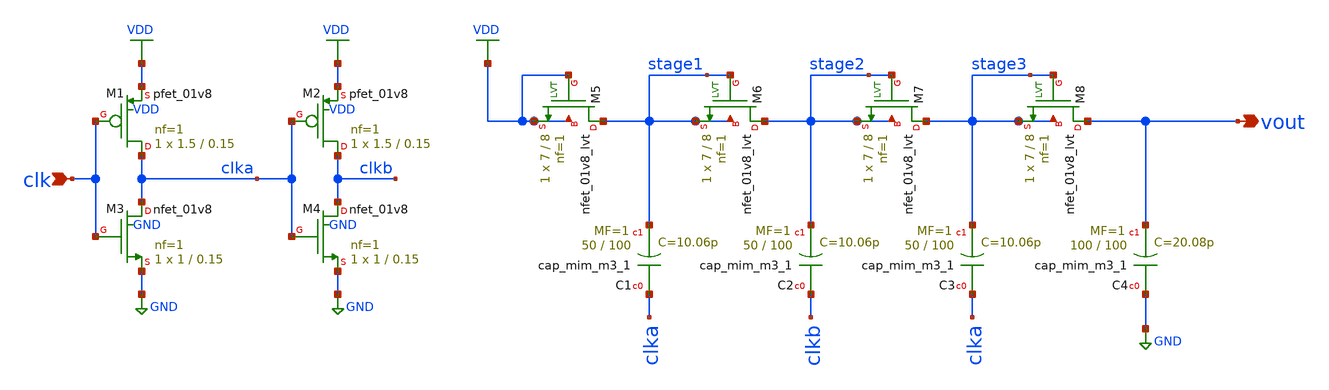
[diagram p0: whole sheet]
** sch_path: xschem/dickson.sch
**.subckt dickson clk vout
*.ipin clk
*.opin vout
XM1 clka clk VDD VDD sky130_fd_pr__pfet_01v8 L=0.15 W=1.5 nf=1 ad='int((nf+1)/2) * W/nf * 0.29' as='int((nf+2)/2) * W/nf * 0.29'
+ pd='2*int((nf+1)/2) * (W/nf + 0.29)' ps='2*int((nf+2)/2) * (W/nf + 0.29)' nrd='0.29 / W' nrs='0.29 / W'
+ sa=0 sb=0 sd=0 mult=1 m=1
XM3 clka clk GND GND sky130_fd_pr__nfet_01v8 L=0.15 W=1 nf=1 ad='int((nf+1)/2) * W/nf * 0.29' as='int((nf+2)/2) * W/nf * 0.29'
+ pd='2*int((nf+1)/2) * (W/nf + 0.29)' ps='2*int((nf+2)/2) * (W/nf + 0.29)' nrd='0.29 / W' nrs='0.29 / W'
+ sa=0 sb=0 sd=0 mult=1 m=1
XM2 clkb clka VDD VDD sky130_fd_pr__pfet_01v8 L=0.15 W=1.5 nf=1 ad='int((nf+1)/2) * W/nf * 0.29' as='int((nf+2)/2) * W/nf * 0.29'
+ pd='2*int((nf+1)/2) * (W/nf + 0.29)' ps='2*int((nf+2)/2) * (W/nf + 0.29)' nrd='0.29 / W' nrs='0.29 / W'
+ sa=0 sb=0 sd=0 mult=1 m=1
XM4 clkb clka GND GND sky130_fd_pr__nfet_01v8 L=0.15 W=1 nf=1 ad='int((nf+1)/2) * W/nf * 0.29' as='int((nf+2)/2) * W/nf * 0.29'
+ pd='2*int((nf+1)/2) * (W/nf + 0.29)' ps='2*int((nf+2)/2) * (W/nf + 0.29)' nrd='0.29 / W' nrs='0.29 / W'
+ sa=0 sb=0 sd=0 mult=1 m=1
XC3 clka stage3 sky130_fd_pr__cap_mim_m3_1 W=50 L=100 MF=1 m=1
XM5 stage1 VDD VDD VDD sky130_fd_pr__nfet_01v8_lvt L=8 W=7 nf=1 ad='int((nf+1)/2) * W/nf * 0.29' as='int((nf+2)/2) * W/nf * 0.29'
+ pd='2*int((nf+1)/2) * (W/nf + 0.29)' ps='2*int((nf+2)/2) * (W/nf + 0.29)' nrd='0.29 / W' nrs='0.29 / W'
+ sa=0 sb=0 sd=0 mult=1 m=1
XC1 clka stage1 sky130_fd_pr__cap_mim_m3_1 W=50 L=100 MF=1 m=1
XM6 stage2 stage1 stage1 stage1 sky130_fd_pr__nfet_01v8_lvt L=8 W=7 nf=1 ad='int((nf+1)/2) * W/nf * 0.29'
+ as='int((nf+2)/2) * W/nf * 0.29' pd='2*int((nf+1)/2) * (W/nf + 0.29)' ps='2*int((nf+2)/2) * (W/nf + 0.29)'
+ nrd='0.29 / W' nrs='0.29 / W' sa=0 sb=0 sd=0 mult=1 m=1
XM7 stage3 stage2 stage2 stage2 sky130_fd_pr__nfet_01v8_lvt L=8 W=7 nf=1 ad='int((nf+1)/2) * W/nf * 0.29'
+ as='int((nf+2)/2) * W/nf * 0.29' pd='2*int((nf+1)/2) * (W/nf + 0.29)' ps='2*int((nf+2)/2) * (W/nf + 0.29)'
+ nrd='0.29 / W' nrs='0.29 / W' sa=0 sb=0 sd=0 mult=1 m=1
XC2 clkb stage2 sky130_fd_pr__cap_mim_m3_1 W=50 L=100 MF=1 m=1
XM8 vout stage3 stage3 stage3 sky130_fd_pr__nfet_01v8_lvt L=8 W=7 nf=1 ad='int((nf+1)/2) * W/nf * 0.29'
+ as='int((nf+2)/2) * W/nf * 0.29' pd='2*int((nf+1)/2) * (W/nf + 0.29)' ps='2*int((nf+2)/2) * (W/nf + 0.29)'
+ nrd='0.29 / W' nrs='0.29 / W' sa=0 sb=0 sd=0 mult=1 m=1
XC4 GND vout sky130_fd_pr__cap_mim_m3_1 W=100 L=100 MF=1 m=1
**.ends
.GLOBAL GND
.GLOBAL VDD
.end
